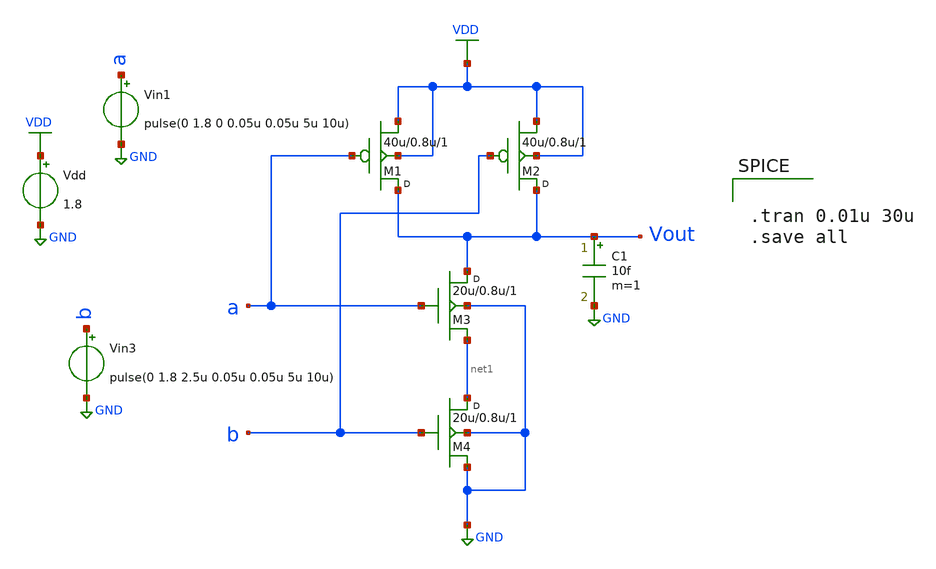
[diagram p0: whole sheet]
** sch_path: cells/nand2/NAND.sch
**.subckt NAND
M3 Vout a net1 GND n1 w=20u l=0.8u m=1
M4 net1 b GND GND n1 w=20u l=0.8u m=1
Vdd VDD GND 1.8
M1 Vout a VDD VDD p1 w=40u l=0.8u m=1
M2 Vout b VDD VDD p1 w=40u l=0.8u m=1
Vin1 a GND pulse(0 1.8 0 0.05u 0.05u 5u 10u)
Vin3 b GND pulse(0 1.8 2.5u 0.05u 0.05u 5u 10u)
C1 Vout GND 10f m=1
**** begin user architecture code


.model n1 nmos level=49 version=3.3.0
.model p1 pmos level=49 version=3.3.0



.tran 0.01u 30u
.save all

**** end user architecture code
**.ends
.GLOBAL GND
.GLOBAL VDD
.end
